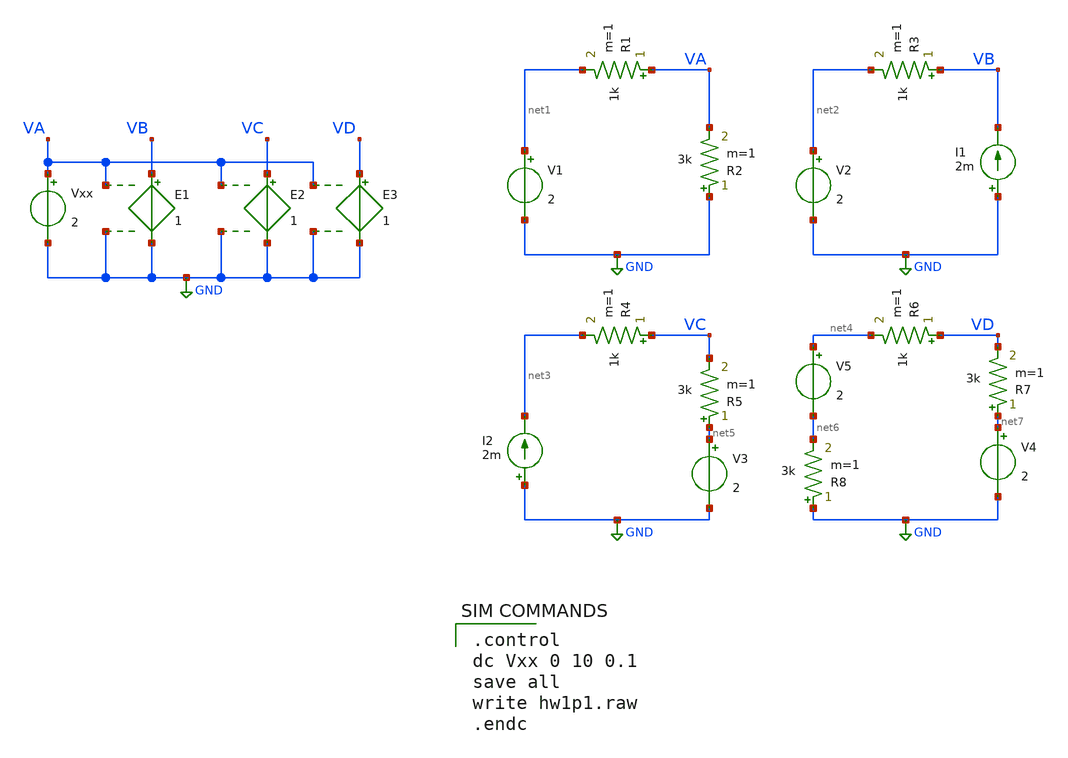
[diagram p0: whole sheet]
** sch_path: hw1p1.sch
**.subckt hw1p1
V1 net1 GND 2
R1 VA net1 1k m=1
R2 GND VA 3k m=1
V2 net2 GND 2
R3 VB net2 1k m=1
I2 GND net3 2m
V3 net5 GND 2
R4 VC net3 1k m=1
R5 net5 VC 3k m=1
V4 net7 GND 2
R6 VD net4 1k m=1
I1 GND VB 2m
R7 net7 VD 3k m=1
R8 GND net6 3k m=1
V5 net4 net6 2
Vxx VA GND 2
E1 VB GND VA GND 1
E2 VC GND VA GND 1
E3 VD GND VA GND 1
**** begin user architecture code

.control
dc Vxx 0 10 0.1
save all
write hw1p1.raw
.endc


**** end user architecture code
**.ends
.GLOBAL GND
.end
